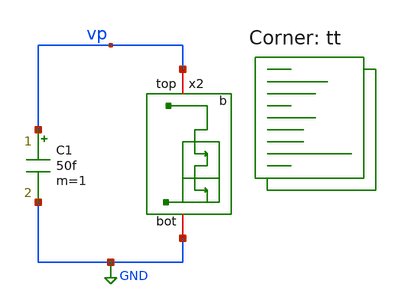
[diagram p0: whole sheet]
** sch_path: xschem/tb/dschr_nwk_type_b_tb.sch
**.subckt dschr_nwk_type_b_tb
C1 vp GND 50f m=1
x2 vp GND dschr_nwk_type_b L=0.15 W=0.5
**** begin user architecture code
.lib $::SKYWATER_MODELS/sky130.lib.spice tt


.include $::netlist_dir/ctrl_sims.spice


**** end user architecture code
**.ends
.GLOBAL GND
.end
